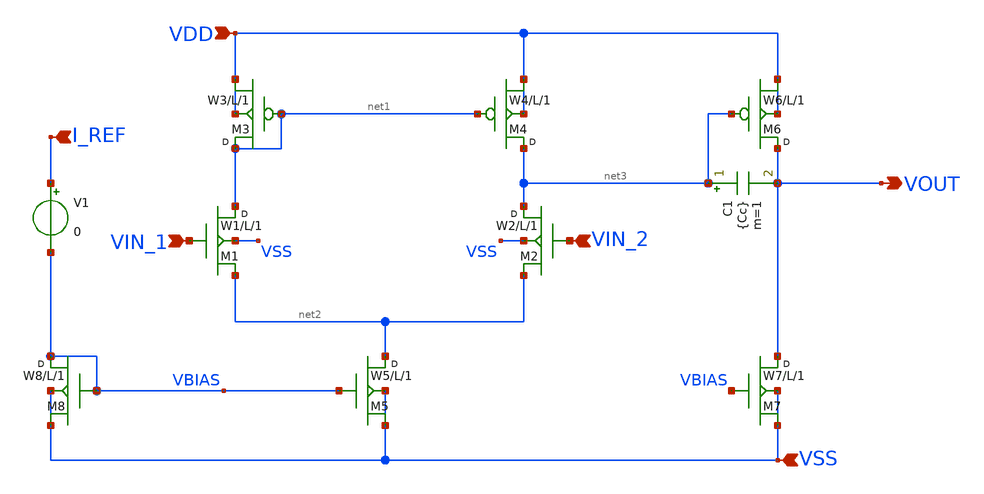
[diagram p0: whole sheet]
** sch_path: schematic/opamp_scheme.sch
**.subckt opamp_scheme VOUT VIN_1 VIN_2 I_REF VDD VSS
*.opin VOUT
*.ipin VIN_1
*.ipin VIN_2
*.ipin I_REF
*.ipin VDD
*.ipin VSS
V1 I_REF VBIAS 0
C1 net3 VOUT {Cc} m=1
M1 net1 VIN_1 net2 VSS N_1u w=W1 l=L m=1
M2 net3 VIN_2 net2 VSS N_1u w=W2 l=L m=1
M3 net1 net1 VDD VDD P_1u w=W3 l=L m=1
M4 net3 net1 VDD VDD P_1u w=W4 l=L m=1
M5 net2 VBIAS VSS VSS N_1u w=W5 l=L m=1
M6 VOUT net3 VDD VDD P_1u w=W6 l=L m=1
M7 VOUT VBIAS VSS VSS N_1u w=W7 l=L m=1
M8 VBIAS VBIAS VSS VSS N_1u w=W8 l=L m=1
**.ends
.end
